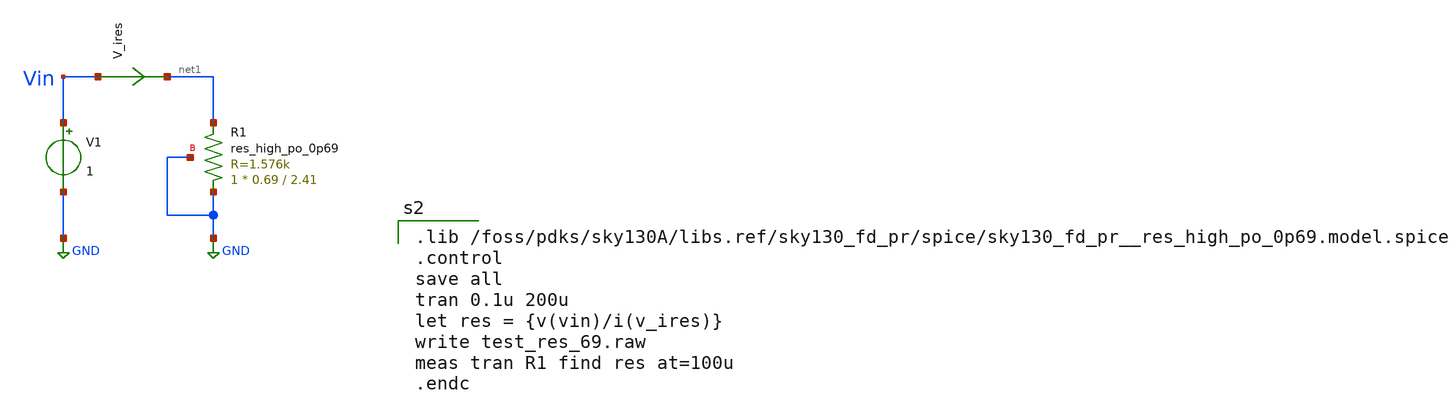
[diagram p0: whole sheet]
** sch_path: xschem/test_res_69.sch
**.subckt test_res_69
XR1 GND net1 GND sky130_fd_pr__res_high_po_0p69 L=2.41 mult=1 m=1
V1 Vin GND 1
V_ires Vin net1 0
.save i(v_ires)
**** begin user architecture code

.lib /foss/pdks/sky130A/libs.ref/sky130_fd_pr/spice/sky130_fd_pr__res_high_po_0p69.model.spice
.control
save all
tran 0.1u 200u
let res = {v(vin)/i(v_ires)}
write test_res_69.raw
meas tran R1 find res at=100u
.endc


** opencircuitdesign pdks install
.lib $::SKYWATER_MODELS/sky130.lib.spice tt


**** end user architecture code
**.ends
.GLOBAL GND
.end
